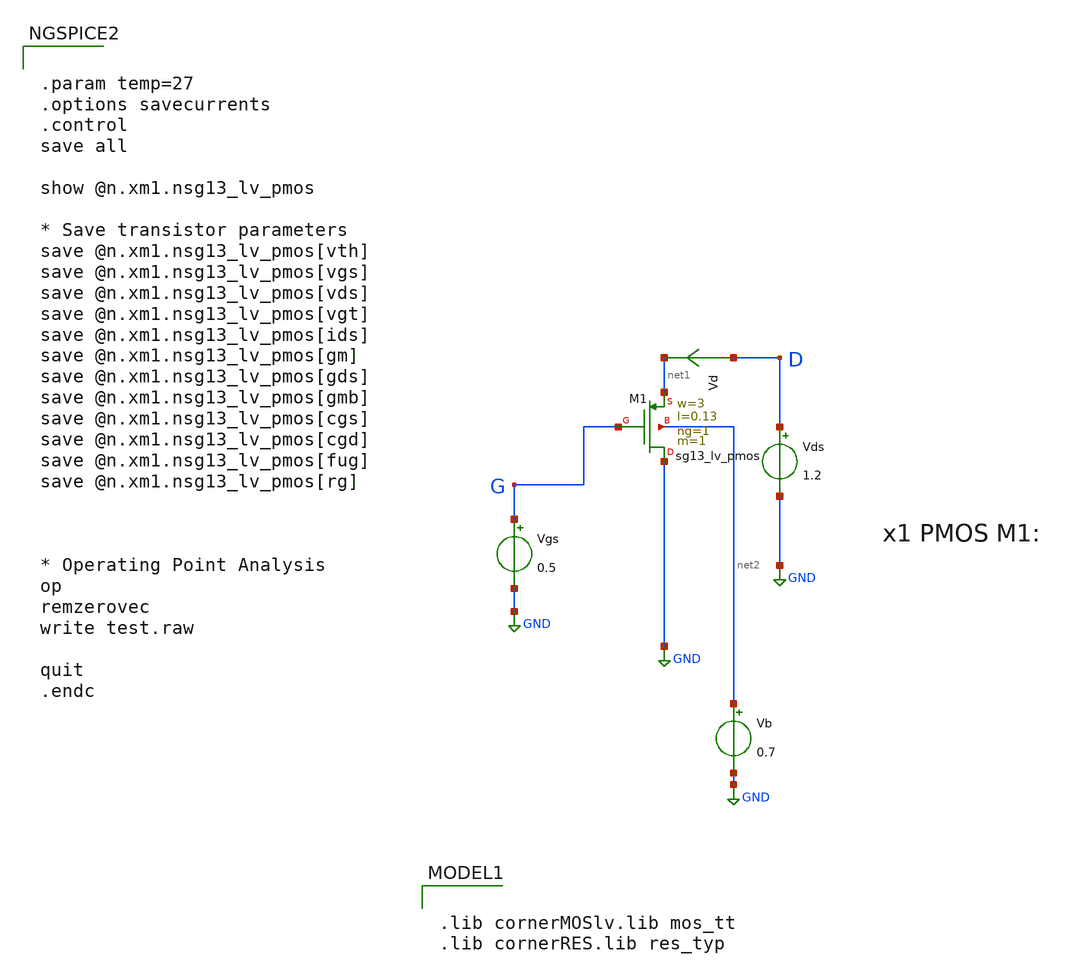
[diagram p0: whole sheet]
** sch_path: xschem/test.sch
**.subckt test
Vgs G GND 0.5
Vds D GND 1.2
Vd D net1 0
.save i(vd)
Vb net2 GND 0.7
XM1 GND G net1 net2 sg13_lv_pmos w=3 l=0.13 ng=1 m=1 mm_ok=1
**** begin user architecture code

.lib cornerMOSlv.lib mos_tt
.lib cornerRES.lib res_typ



.param temp=27
.options savecurrents
.control
save all

show @n.xm1.nsg13_lv_pmos

* Save transistor parameters
save @n.xm1.nsg13_lv_pmos[vth]
save @n.xm1.nsg13_lv_pmos[vgs]
save @n.xm1.nsg13_lv_pmos[vds]
save @n.xm1.nsg13_lv_pmos[vgt]
save @n.xm1.nsg13_lv_pmos[ids]
save @n.xm1.nsg13_lv_pmos[gm]
save @n.xm1.nsg13_lv_pmos[gds]
save @n.xm1.nsg13_lv_pmos[gmb]
save @n.xm1.nsg13_lv_pmos[cgs]
save @n.xm1.nsg13_lv_pmos[cgd]
save @n.xm1.nsg13_lv_pmos[fug]
save @n.xm1.nsg13_lv_pmos[rg]



* Operating Point Analysis
op
remzerovec
write test.raw

quit
.endc

**** end user architecture code
**.ends
.GLOBAL GND
.end
